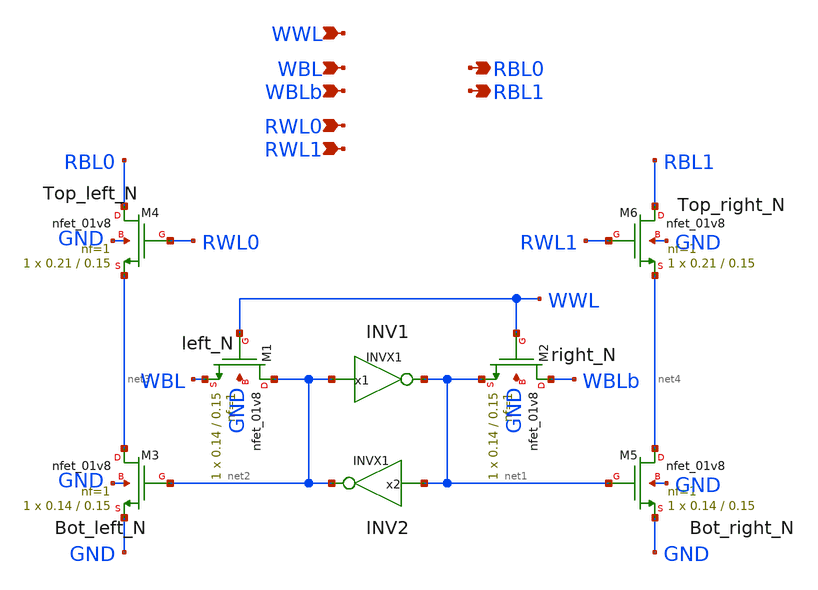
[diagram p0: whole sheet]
** sch_path: custom/xschem/10T_toy_xschem.sch
**.subckt 10T_toy_xschem WWL RWL0 RWL1 WBL WBLb RBL0 RBL1
*.ipin WWL
*.ipin RWL0
*.ipin RWL1
*.ipin WBL
*.ipin WBLb
*.opin RBL0
*.opin RBL1
x1 net1 net2 VDD GND INVX1
x2 net2 net1 VDD GND INVX1
XM1 net2 WWL WBL GND sky130_fd_pr__nfet_01v8 L=0.15 W=0.14 nf=1 ad='int((nf+1)/2) * W/nf * 0.29' as='int((nf+2)/2) * W/nf * 0.29'
+ pd='2*int((nf+1)/2) * (W/nf + 0.29)' ps='2*int((nf+2)/2) * (W/nf + 0.29)' nrd='0.29 / W' nrs='0.29 / W'
+ sa=0 sb=0 sd=0 mult=1 m=1
XM2 WBLb WWL net1 GND sky130_fd_pr__nfet_01v8 L=0.15 W=0.14 nf=1 ad='int((nf+1)/2) * W/nf * 0.29' as='int((nf+2)/2) * W/nf * 0.29'
+ pd='2*int((nf+1)/2) * (W/nf + 0.29)' ps='2*int((nf+2)/2) * (W/nf + 0.29)' nrd='0.29 / W' nrs='0.29 / W'
+ sa=0 sb=0 sd=0 mult=1 m=1
XM3 net3 net2 GND GND sky130_fd_pr__nfet_01v8 L=0.15 W=0.14 nf=1 ad='int((nf+1)/2) * W/nf * 0.29' as='int((nf+2)/2) * W/nf * 0.29'
+ pd='2*int((nf+1)/2) * (W/nf + 0.29)' ps='2*int((nf+2)/2) * (W/nf + 0.29)' nrd='0.29 / W' nrs='0.29 / W'
+ sa=0 sb=0 sd=0 mult=1 m=1
XM4 RBL0 RWL0 net3 GND sky130_fd_pr__nfet_01v8 L=0.15 W=0.21 nf=1 ad='int((nf+1)/2) * W/nf * 0.29' as='int((nf+2)/2) * W/nf * 0.29'
+ pd='2*int((nf+1)/2) * (W/nf + 0.29)' ps='2*int((nf+2)/2) * (W/nf + 0.29)' nrd='0.29 / W' nrs='0.29 / W'
+ sa=0 sb=0 sd=0 mult=1 m=1
XM5 net4 net1 GND GND sky130_fd_pr__nfet_01v8 L=0.15 W=0.14 nf=1 ad='int((nf+1)/2) * W/nf * 0.29' as='int((nf+2)/2) * W/nf * 0.29'
+ pd='2*int((nf+1)/2) * (W/nf + 0.29)' ps='2*int((nf+2)/2) * (W/nf + 0.29)' nrd='0.29 / W' nrs='0.29 / W'
+ sa=0 sb=0 sd=0 mult=1 m=1
XM6 RBL1 RWL1 net4 GND sky130_fd_pr__nfet_01v8 L=0.15 W=0.21 nf=1 ad='int((nf+1)/2) * W/nf * 0.29' as='int((nf+2)/2) * W/nf * 0.29'
+ pd='2*int((nf+1)/2) * (W/nf + 0.29)' ps='2*int((nf+2)/2) * (W/nf + 0.29)' nrd='0.29 / W' nrs='0.29 / W'
+ sa=0 sb=0 sd=0 mult=1 m=1
**.ends

* expanding   symbol:  INVX1.sym # of pins=2
** sym_path: custom/xschem/INVX1.sym
** sch_path: custom/xschem/INVX1.sch
.subckt INVX1 Y A VDD GND
*.ipin A
*.opin Y
XM1 Y A GND GND sky130_fd_pr__nfet_01v8 L=0.15 W=0.21 nf=1 ad='int((nf+1)/2) * W/nf * 0.29' as='int((nf+2)/2) * W/nf * 0.29'
+ pd='2*int((nf+1)/2) * (W/nf + 0.29)' ps='2*int((nf+2)/2) * (W/nf + 0.29)' nrd='0.29 / W' nrs='0.29 / W'
+ sa=0 sb=0 sd=0 mult=1 m=1
XM2 Y A VDD VDD sky130_fd_pr__pfet_01v8 L=0.15 W=0.14 nf=1 ad='int((nf+1)/2) * W/nf * 0.29' as='int((nf+2)/2) * W/nf * 0.29'
+ pd='2*int((nf+1)/2) * (W/nf + 0.29)' ps='2*int((nf+2)/2) * (W/nf + 0.29)' nrd='0.29 / W' nrs='0.29 / W'
+ sa=0 sb=0 sd=0 mult=1 m=1
.ends

.end
